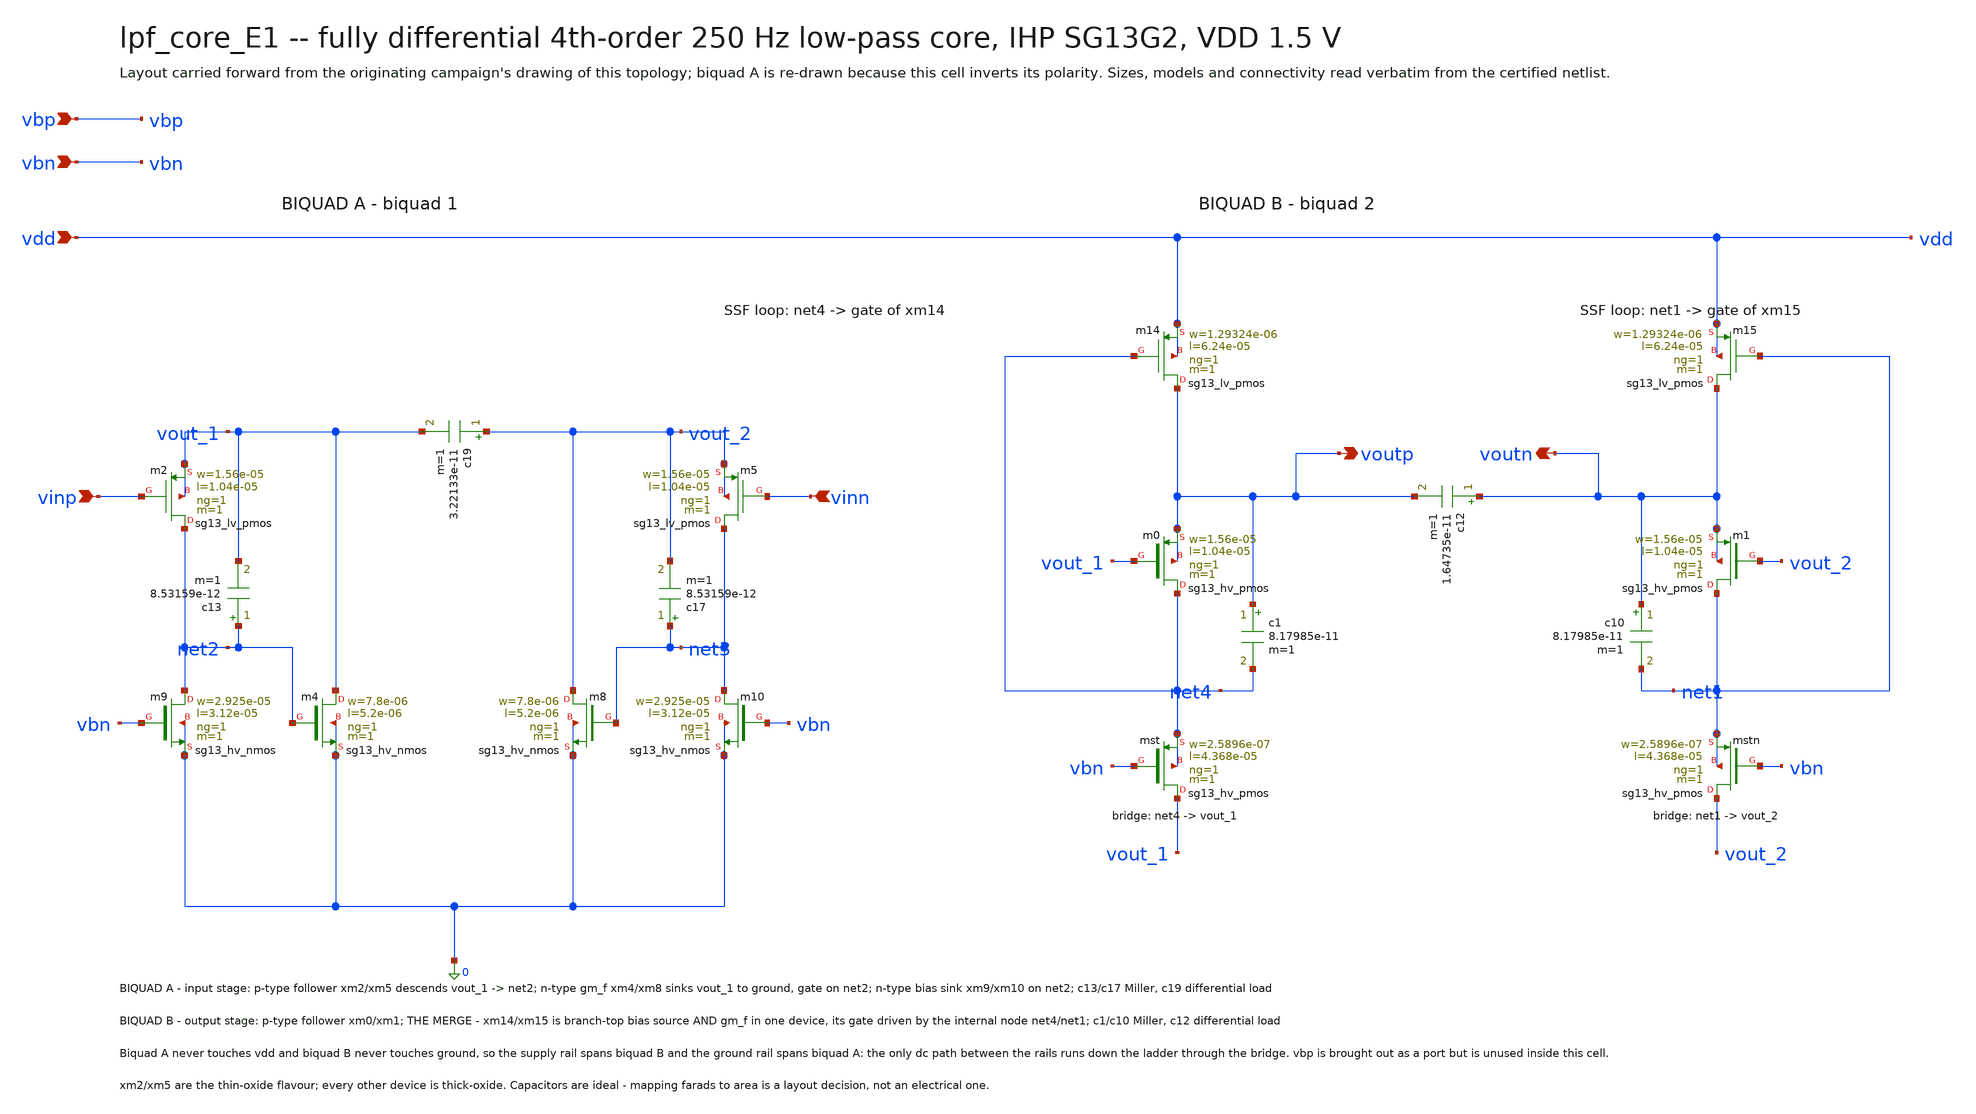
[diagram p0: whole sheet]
** sch_path: signoff/E1-prev/lpf_core_E1.sch
**.subckt lpf_core_E1 vinp vinn voutp voutn vdd vbn vbp
*.ipin vinp
*.ipin vinn
*.opin voutp
*.opin voutn
*.ipin vdd
*.ipin vbn
*.ipin vbp
Xm2 net2 vinp vout_1 vout_1 sg13_lv_pmos w=1.56e-05 l=1.04e-05 ng=1 m=1 mm_ok=1
Xm5 net3 vinn vout_2 vout_2 sg13_lv_pmos w=1.56e-05 l=1.04e-05 ng=1 m=1 mm_ok=1
Xm4 vout_1 net2 0 0 sg13_hv_nmos w=7.8e-06 l=5.2e-06 ng=1 m=1 mm_ok=1
Xm8 vout_2 net3 0 0 sg13_hv_nmos w=7.8e-06 l=5.2e-06 ng=1 m=1 mm_ok=1
Xm9 net2 vbn 0 0 sg13_hv_nmos w=2.925e-05 l=3.12e-05 ng=1 m=1 mm_ok=1
Xm10 net3 vbn 0 0 sg13_hv_nmos w=2.925e-05 l=3.12e-05 ng=1 m=1 mm_ok=1
Xmst vout_1 vbn net4 net4 sg13_hv_pmos w=2.5896e-07 l=4.368e-05 ng=1 m=1 mm_ok=1
Xmstn vout_2 vbn net1 net1 sg13_hv_pmos w=2.5896e-07 l=4.368e-05 ng=1 m=1 mm_ok=1
Xm0 net4 vout_1 voutp voutp sg13_hv_pmos w=1.56e-05 l=1.04e-05 ng=1 m=1 mm_ok=1
Xm1 net1 vout_2 voutn voutn sg13_hv_pmos w=1.56e-05 l=1.04e-05 ng=1 m=1 mm_ok=1
Xm14 voutp net4 vdd vdd sg13_lv_pmos w=1.29324e-06 l=6.24e-05 ng=1 m=1 mm_ok=1
Xm15 voutn net1 vdd vdd sg13_lv_pmos w=1.29324e-06 l=6.24e-05 ng=1 m=1 mm_ok=1
c13 net2 vout_1 8.53159e-12 m=1
c17 net3 vout_2 8.53159e-12 m=1
c19 vout_2 vout_1 3.22133e-11 m=1
c1 voutp net4 8.17985e-11 m=1
c10 voutn net1 8.17985e-11 m=1
c12 voutn voutp 1.64735e-11 m=1
**.ends
.end
